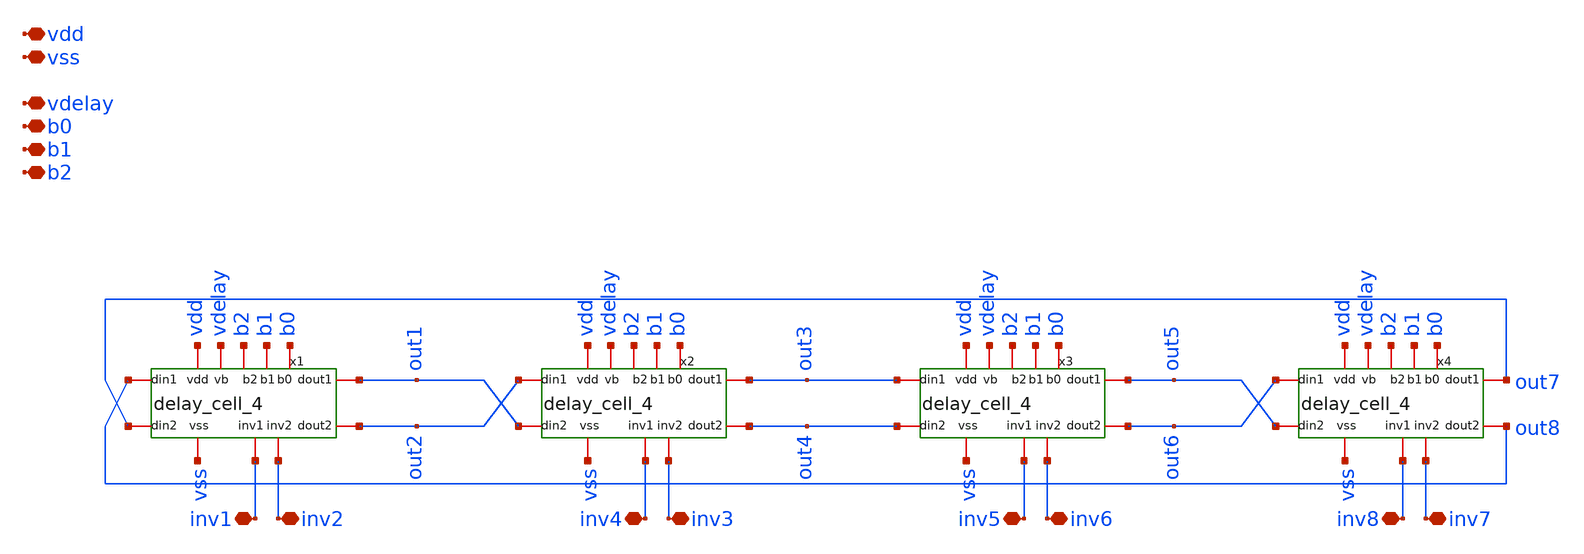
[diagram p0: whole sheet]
** sch_path: xschem/vco_core_8.sch
**.subckt vco_core_8 vdd vss vdelay b0 b1 b2 inv1 inv2 inv3 inv4 inv5 inv6 inv7 inv8
*.iopin vdd
*.iopin vss
*.iopin vdelay
*.iopin b0
*.iopin b1
*.iopin b2
*.iopin inv1
*.iopin inv2
*.iopin inv3
*.iopin inv4
*.iopin inv5
*.iopin inv6
*.iopin inv7
*.iopin inv8
x1 vdd vdelay out2 out1 out7 out8 vss b2 b1 b0 inv2 inv1 delay_cell_4
x2 vdd vdelay out4 out3 out1 out2 vss b2 b1 b0 inv3 inv4 delay_cell_4
x3 vdd vdelay out6 out5 out4 out3 vss b2 b1 b0 inv6 inv5 delay_cell_4
x4 vdd vdelay out8 out7 out5 out6 vss b2 b1 b0 inv7 inv8 delay_cell_4
**.ends
.end
